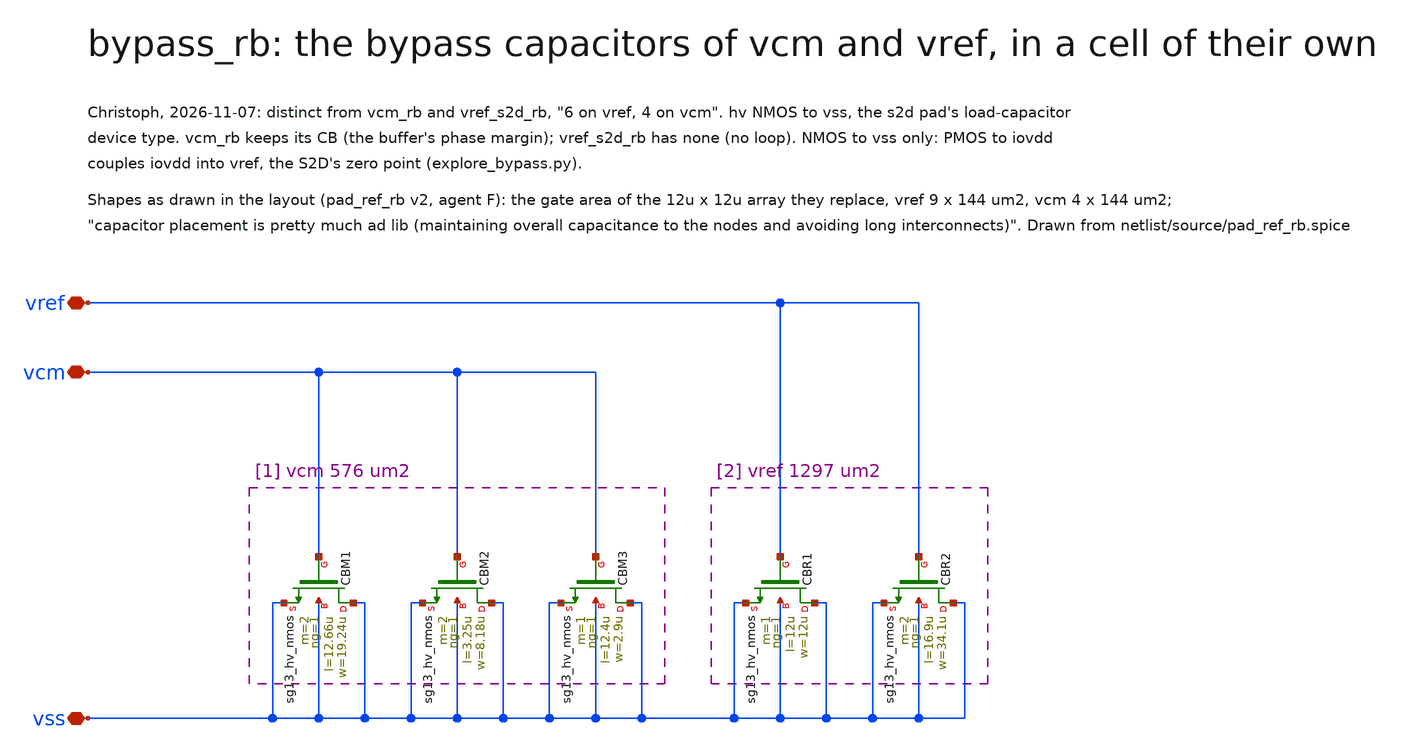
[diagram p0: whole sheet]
** sch_path: macros/pad_ref_rb/schematic/xschem/bypass_rb.sch
**.subckt bypass_rb vss vcm vref
*.iopin vss
*.iopin vcm
*.iopin vref
XCBM1 vss vcm vss vss sg13_hv_nmos w=19.24u l=12.66u ng=1 m=2 mm_ok=1
XCBM2 vss vcm vss vss sg13_hv_nmos w=8.18u l=3.25u ng=1 m=2 mm_ok=1
XCBM3 vss vcm vss vss sg13_hv_nmos w=2.9u l=12.4u ng=1 m=1 mm_ok=1
XCBR1 vss vref vss vss sg13_hv_nmos w=12u l=12u ng=1 m=1 mm_ok=1
XCBR2 vss vref vss vss sg13_hv_nmos w=34.1u l=16.9u ng=1 m=2 mm_ok=1
**.ends
.end
